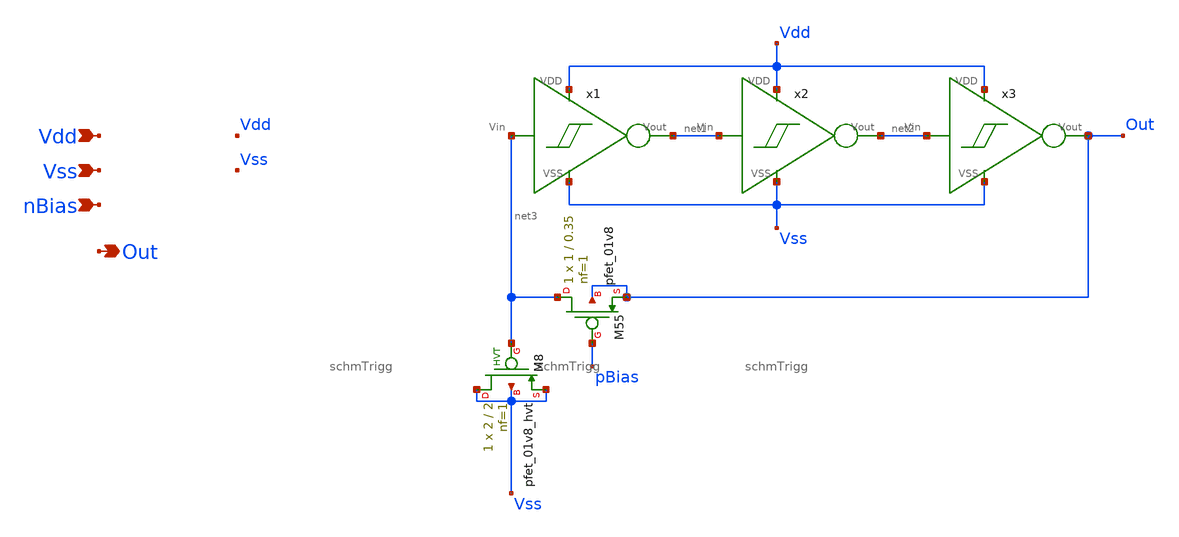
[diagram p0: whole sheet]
** sch_path: xschem/T3/oscillators/A_tt10_Ring_currentStarved/osc.sch
**.subckt osc Vdd Vss Out nBias
*.ipin Vdd
*.ipin Vss
*.opin Out
*.ipin nBias
x1 net3 Vss Vdd net1 schmTrigg
x2 net1 Vss Vdd net2 schmTrigg
x3 net2 Vss Vdd Out schmTrigg
XM55 net3 pBias Out Out sky130_fd_pr__pfet_01v8 L=0.35 W=1 nf=1 ad='int((nf+1)/2) * W/nf * 0.29' as='int((nf+2)/2) * W/nf * 0.29'
+ pd='2*int((nf+1)/2) * (W/nf + 0.29)' ps='2*int((nf+2)/2) * (W/nf + 0.29)' nrd='0.29 / W' nrs='0.29 / W'
+ sa=0 sb=0 sd=0 mult=1 m=1
XM8 Vss net3 Vss Vss sky130_fd_pr__pfet_01v8_hvt L=2 W=2 nf=1 ad='int((1 + 1)/2) * 2 / 1 * 0.29' as='int((1 + 2)/2) * 2 / 1 * 0.29'
+ pd='2*int((1 + 1)/2) * (2 / 1 + 0.29)' ps='2*int((1 + 2)/2) * (2 / 1 + 0.29)' nrd='0.29 / 2 ' nrs='0.29 / 2 '
+ sa=0 sb=0 sd=0 mult=1 m=1
**.ends

* expanding   symbol:  T1/schmTrigg/schmTrigg.sym # of pins=4
** sym_path: xschem/T1/schmTrigg/schmTrigg.sym
** sch_path: xschem/T1/schmTrigg/schmTrigg.sch
.subckt schmTrigg Vin VSS VDD Vout
*.ipin Vin
*.ipin VDD
*.ipin VSS
*.opin Vout
XM1 VDD Vout Vn Vn sky130_fd_pr__nfet_01v8 L=0.15 W=1 nf=1 ad='int((1 + 1)/2) * 1 / 1 * 0.29' as='int((1 + 2)/2) * 1 / 1 * 0.29'
+ pd='2*int((1 + 1)/2) * (1 / 1 + 0.29)' ps='2*int((1 + 2)/2) * (1 / 1 + 0.29)' nrd='0.29 / 1 ' nrs='0.29 / 1 '
+ sa=0 sb=0 sd=0 mult=1 m=1
XM2 Vn Vin VSS VSS sky130_fd_pr__nfet_01v8 L=0.15 W=1 nf=1 ad='int((1 + 1)/2) * 1 / 1 * 0.29' as='int((1 + 2)/2) * 1 / 1 * 0.29'
+ pd='2*int((1 + 1)/2) * (1 / 1 + 0.29)' ps='2*int((1 + 2)/2) * (1 / 1 + 0.29)' nrd='0.29 / 1 ' nrs='0.29 / 1 '
+ sa=0 sb=0 sd=0 mult=1 m=1
XM3 Vout Vin Vn Vn sky130_fd_pr__nfet_01v8 L=0.15 W=1 nf=1 ad='int((1 + 1)/2) * 1 / 1 * 0.29' as='int((1 + 2)/2) * 1 / 1 * 0.29'
+ pd='2*int((1 + 1)/2) * (1 / 1 + 0.29)' ps='2*int((1 + 2)/2) * (1 / 1 + 0.29)' nrd='0.29 / 1 ' nrs='0.29 / 1 '
+ sa=0 sb=0 sd=0 mult=1 m=1
XM4 VSS Vout Vp Vp sky130_fd_pr__pfet_01v8 L=0.15 W=1 nf=1 ad='int((nf+1)/2) * W/nf * 0.29' as='int((nf+2)/2) * W/nf * 0.29'
+ pd='2*int((nf+1)/2) * (W/nf + 0.29)' ps='2*int((nf+2)/2) * (W/nf + 0.29)' nrd='0.29 / W' nrs='0.29 / W'
+ sa=0 sb=0 sd=0 mult=1 m=1
XM5 Vout Vin Vp Vp sky130_fd_pr__pfet_01v8 L=0.15 W=1 nf=1 ad='int((nf+1)/2) * W/nf * 0.29' as='int((nf+2)/2) * W/nf * 0.29'
+ pd='2*int((nf+1)/2) * (W/nf + 0.29)' ps='2*int((nf+2)/2) * (W/nf + 0.29)' nrd='0.29 / W' nrs='0.29 / W'
+ sa=0 sb=0 sd=0 mult=1 m=1
XM6 Vp Vin VDD VDD sky130_fd_pr__pfet_01v8 L=0.15 W=1 nf=1 ad='int((nf+1)/2) * W/nf * 0.29' as='int((nf+2)/2) * W/nf * 0.29'
+ pd='2*int((nf+1)/2) * (W/nf + 0.29)' ps='2*int((nf+2)/2) * (W/nf + 0.29)' nrd='0.29 / W' nrs='0.29 / W'
+ sa=0 sb=0 sd=0 mult=1 m=1
.ends

.end
